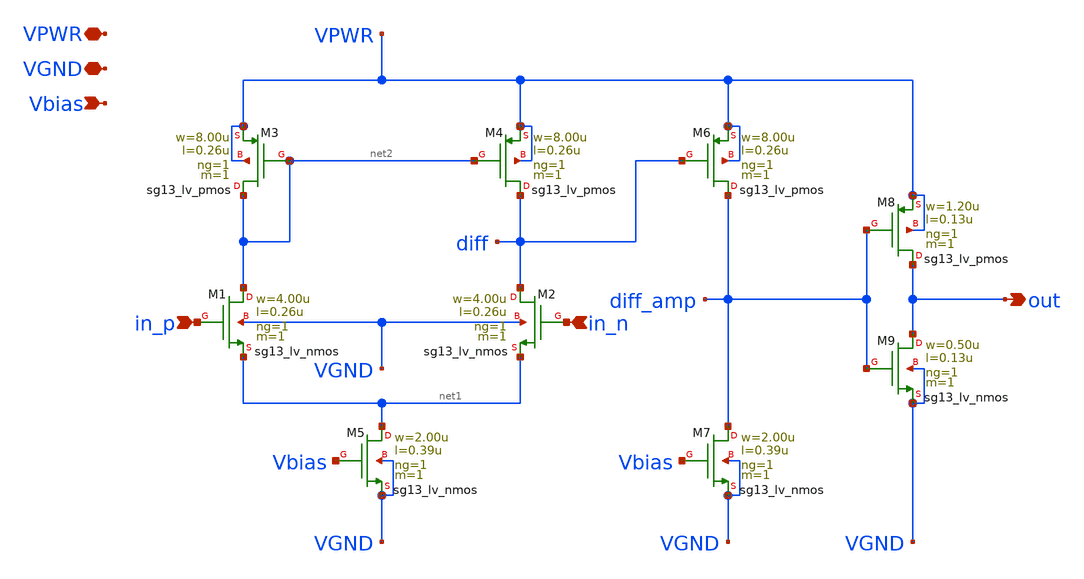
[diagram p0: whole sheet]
** sch_path: xschem/comparator.sch
**.subckt comparator VPWR in_p in_n out VGND Vbias
*.iopin VPWR
*.ipin in_p
*.ipin in_n
*.opin out
*.iopin VGND
*.ipin Vbias
XM1 net2 in_p net1 VGND sg13_lv_nmos w=4.00u l=0.26u ng=1 m=1 mm_ok=1
XM4 diff net2 VPWR VPWR sg13_lv_pmos w=8.00u l=0.26u ng=1 m=1 mm_ok=1
XM5 net1 Vbias VGND VGND sg13_lv_nmos w=2.00u l=0.39u ng=1 m=1 mm_ok=1
XM2 diff in_n net1 VGND sg13_lv_nmos w=4.00u l=0.26u ng=1 m=1 mm_ok=1
XM3 net2 net2 VPWR VPWR sg13_lv_pmos w=8.00u l=0.26u ng=1 m=1 mm_ok=1
XM6 diff_amp diff VPWR VPWR sg13_lv_pmos w=8.00u l=0.26u ng=1 m=1 mm_ok=1
XM7 diff_amp Vbias VGND VGND sg13_lv_nmos w=2.00u l=0.39u ng=1 m=1 mm_ok=1
XM8 out diff_amp VPWR VPWR sg13_lv_pmos w=1.20u l=0.13u ng=1 m=1 mm_ok=1
XM9 out diff_amp VGND VGND sg13_lv_nmos w=0.50u l=0.13u ng=1 m=1 mm_ok=1
**.ends
.end
